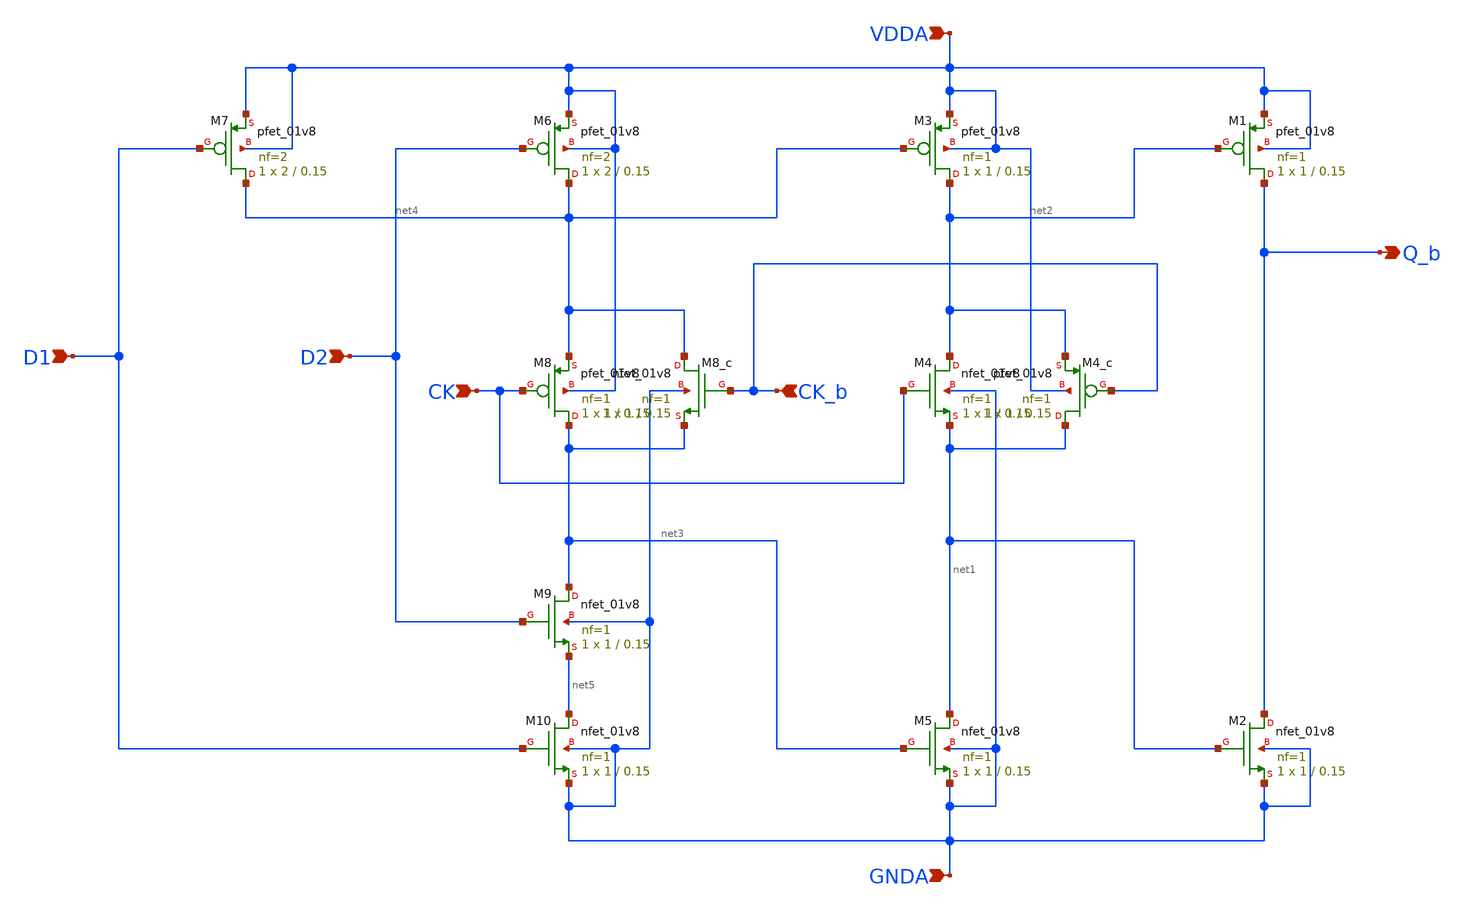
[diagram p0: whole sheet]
** sch_path: projects/pll/divider/xschem_ngspice/TSPC_FF_comp_sw_nand.sch
**.subckt TSPC_FF_comp_sw_nand CK D1 Q_b VDDA GNDA CK_b D2
*.ipin CK
*.ipin D1
*.opin Q_b
*.ipin VDDA
*.ipin GNDA
*.ipin CK_b
*.ipin D2
XM1 Q_b net2 VDDA VDDA sky130_fd_pr__pfet_01v8 L=0.15 W=1 nf=1 ad='int((nf+1)/2) * W/nf * 0.29' as='int((nf+2)/2) * W/nf * 0.29'
+ pd='2*int((nf+1)/2) * (W/nf + 0.29)' ps='2*int((nf+2)/2) * (W/nf + 0.29)' nrd='0.29 / W' nrs='0.29 / W'
+ sa=0 sb=0 sd=0 mult=1 m=1
XM4 net2 CK net1 GNDA sky130_fd_pr__nfet_01v8 L=0.15 W=1 nf=1 ad='int((nf+1)/2) * W/nf * 0.29' as='int((nf+2)/2) * W/nf * 0.29'
+ pd='2*int((nf+1)/2) * (W/nf + 0.29)' ps='2*int((nf+2)/2) * (W/nf + 0.29)' nrd='0.29 / W' nrs='0.29 / W'
+ sa=0 sb=0 sd=0 mult=1 m=1
XM2 Q_b net1 GNDA GNDA sky130_fd_pr__nfet_01v8 L=0.15 W=1 nf=1 ad='int((nf+1)/2) * W/nf * 0.29' as='int((nf+2)/2) * W/nf * 0.29'
+ pd='2*int((nf+1)/2) * (W/nf + 0.29)' ps='2*int((nf+2)/2) * (W/nf + 0.29)' nrd='0.29 / W' nrs='0.29 / W'
+ sa=0 sb=0 sd=0 mult=1 m=1
XM3 net2 net4 VDDA VDDA sky130_fd_pr__pfet_01v8 L=0.15 W=1 nf=1 ad='int((nf+1)/2) * W/nf * 0.29' as='int((nf+2)/2) * W/nf * 0.29'
+ pd='2*int((nf+1)/2) * (W/nf + 0.29)' ps='2*int((nf+2)/2) * (W/nf + 0.29)' nrd='0.29 / W' nrs='0.29 / W'
+ sa=0 sb=0 sd=0 mult=1 m=1
XM5 net1 net3 GNDA GNDA sky130_fd_pr__nfet_01v8 L=0.15 W=1 nf=1 ad='int((nf+1)/2) * W/nf * 0.29' as='int((nf+2)/2) * W/nf * 0.29'
+ pd='2*int((nf+1)/2) * (W/nf + 0.29)' ps='2*int((nf+2)/2) * (W/nf + 0.29)' nrd='0.29 / W' nrs='0.29 / W'
+ sa=0 sb=0 sd=0 mult=1 m=1
XM6 net4 D2 VDDA VDDA sky130_fd_pr__pfet_01v8 L=0.15 W=2 nf=2 ad='int((nf+1)/2) * W/nf * 0.29' as='int((nf+2)/2) * W/nf * 0.29'
+ pd='2*int((nf+1)/2) * (W/nf + 0.29)' ps='2*int((nf+2)/2) * (W/nf + 0.29)' nrd='0.29 / W' nrs='0.29 / W'
+ sa=0 sb=0 sd=0 mult=1 m=1
XM10 net5 D1 GNDA GNDA sky130_fd_pr__nfet_01v8 L=0.15 W=1 nf=1 ad='int((nf+1)/2) * W/nf * 0.29' as='int((nf+2)/2) * W/nf * 0.29'
+ pd='2*int((nf+1)/2) * (W/nf + 0.29)' ps='2*int((nf+2)/2) * (W/nf + 0.29)' nrd='0.29 / W' nrs='0.29 / W'
+ sa=0 sb=0 sd=0 mult=1 m=1
XM8 net3 CK net4 VDDA sky130_fd_pr__pfet_01v8 L=0.15 W=1 nf=1 ad='int((nf+1)/2) * W/nf * 0.29' as='int((nf+2)/2) * W/nf * 0.29'
+ pd='2*int((nf+1)/2) * (W/nf + 0.29)' ps='2*int((nf+2)/2) * (W/nf + 0.29)' nrd='0.29 / W' nrs='0.29 / W'
+ sa=0 sb=0 sd=0 mult=1 m=1
XM4_c net1 CK_b net2 VDDA sky130_fd_pr__pfet_01v8 L=0.15 W=1 nf=1 ad='int((nf+1)/2) * W/nf * 0.29' as='int((nf+2)/2) * W/nf * 0.29'
+ pd='2*int((nf+1)/2) * (W/nf + 0.29)' ps='2*int((nf+2)/2) * (W/nf + 0.29)' nrd='0.29 / W' nrs='0.29 / W'
+ sa=0 sb=0 sd=0 mult=1 m=1
XM8_c net4 CK_b net3 GNDA sky130_fd_pr__nfet_01v8 L=0.15 W=1 nf=1 ad='int((nf+1)/2) * W/nf * 0.29' as='int((nf+2)/2) * W/nf * 0.29'
+ pd='2*int((nf+1)/2) * (W/nf + 0.29)' ps='2*int((nf+2)/2) * (W/nf + 0.29)' nrd='0.29 / W' nrs='0.29 / W'
+ sa=0 sb=0 sd=0 mult=1 m=1
XM9 net3 D2 net5 GNDA sky130_fd_pr__nfet_01v8 L=0.15 W=1 nf=1 ad='int((nf+1)/2) * W/nf * 0.29' as='int((nf+2)/2) * W/nf * 0.29'
+ pd='2*int((nf+1)/2) * (W/nf + 0.29)' ps='2*int((nf+2)/2) * (W/nf + 0.29)' nrd='0.29 / W' nrs='0.29 / W'
+ sa=0 sb=0 sd=0 mult=1 m=1
XM7 net4 D1 VDDA VDDA sky130_fd_pr__pfet_01v8 L=0.15 W=2 nf=2 ad='int((nf+1)/2) * W/nf * 0.29' as='int((nf+2)/2) * W/nf * 0.29'
+ pd='2*int((nf+1)/2) * (W/nf + 0.29)' ps='2*int((nf+2)/2) * (W/nf + 0.29)' nrd='0.29 / W' nrs='0.29 / W'
+ sa=0 sb=0 sd=0 mult=1 m=1
**.ends
.end
